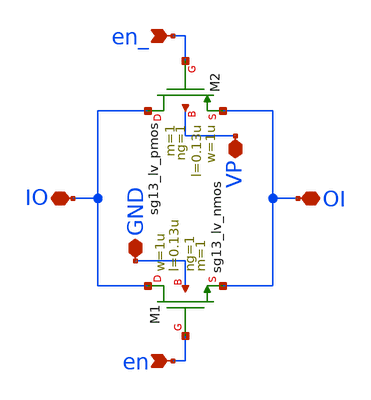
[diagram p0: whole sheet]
** sch_path: schematics/vco/vco_cell/vco_passgate.sch
**.subckt vco_passgate OI IO VP GND en_ en
*.iopin OI
*.iopin IO
*.iopin VP
*.iopin GND
*.ipin en_
*.ipin en
XM1 IO en OI GND sg13_lv_nmos w=1u l=0.13u ng=1 m=1 mm_ok=1
XM2 IO en_ OI VP sg13_lv_pmos w=1u l=0.13u ng=1 m=1 mm_ok=1
**.ends
.end
